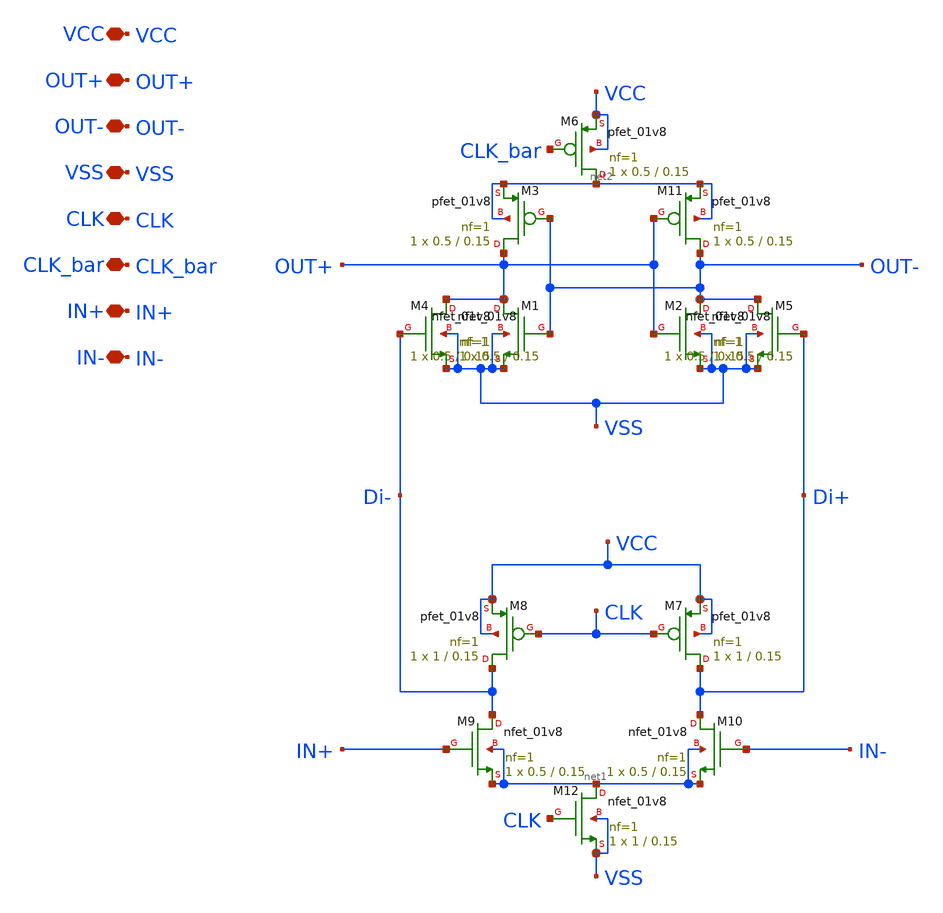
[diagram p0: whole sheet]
** sch_path: voltage_comp/double_tail_comp.sch
**.subckt double_tail_comp OUT- VSS VCC OUT+ IN+ IN- CLK CLK_bar
*.iopin OUT-
*.iopin VSS
*.iopin VCC
*.iopin OUT+
*.iopin IN+
*.iopin IN-
*.iopin CLK
*.iopin CLK_bar
XM2 OUT- OUT+ VSS VSS sky130_fd_pr__nfet_01v8 L=0.15 W=0.5 nf=1 ad='int((1 + 1)/2) * 0.5 / 1 * 0.29'
+ as='int((1 + 2)/2) * 0.5 / 1 * 0.29' pd='2*int((1 + 1)/2) * (0.5 / 1 + 0.29)' ps='2*int((1 + 2)/2) * (0.5 / 1 + 0.29)'
+ nrd='0.29 / 0.5 ' nrs='0.29 / 0.5 ' sa=0 sb=0 sd=0 mult=1 m=1
XM11 OUT- OUT+ net2 net2 sky130_fd_pr__pfet_01v8 L=0.15 W=0.5 nf=1 ad='int((nf+1)/2) * W/nf * 0.29' as='int((nf+2)/2) * W/nf * 0.29'
+ pd='2*int((nf+1)/2) * (W/nf + 0.29)' ps='2*int((nf+2)/2) * (W/nf + 0.29)' nrd='0.29 / W' nrs='0.29 / W'
+ sa=0 sb=0 sd=0 mult=1 m=1
XM1 OUT+ OUT- VSS VSS sky130_fd_pr__nfet_01v8 L=0.15 W=0.5 nf=1 ad='int((1 + 1)/2) * 0.5 / 1 * 0.29'
+ as='int((1 + 2)/2) * 0.5 / 1 * 0.29' pd='2*int((1 + 1)/2) * (0.5 / 1 + 0.29)' ps='2*int((1 + 2)/2) * (0.5 / 1 + 0.29)'
+ nrd='0.29 / 0.5 ' nrs='0.29 / 0.5 ' sa=0 sb=0 sd=0 mult=1 m=1
XM3 OUT+ OUT- net2 net2 sky130_fd_pr__pfet_01v8 L=0.15 W=0.5 nf=1 ad='int((nf+1)/2) * W/nf * 0.29' as='int((nf+2)/2) * W/nf * 0.29'
+ pd='2*int((nf+1)/2) * (W/nf + 0.29)' ps='2*int((nf+2)/2) * (W/nf + 0.29)' nrd='0.29 / W' nrs='0.29 / W'
+ sa=0 sb=0 sd=0 mult=1 m=1
XM4 OUT+ Di- VSS VSS sky130_fd_pr__nfet_01v8 L=0.15 W=0.5 nf=1 ad='int((1 + 1)/2) * 0.5 / 1 * 0.29' as='int((1 + 2)/2) * 0.5 / 1 * 0.29'
+ pd='2*int((1 + 1)/2) * (0.5 / 1 + 0.29)' ps='2*int((1 + 2)/2) * (0.5 / 1 + 0.29)' nrd='0.29 / 0.5 ' nrs='0.29 / 0.5 '
+ sa=0 sb=0 sd=0 mult=1 m=1
XM5 OUT- Di+ VSS VSS sky130_fd_pr__nfet_01v8 L=0.15 W=0.5 nf=1 ad='int((1 + 1)/2) * 0.5 / 1 * 0.29' as='int((1 + 2)/2) * 0.5 / 1 * 0.29'
+ pd='2*int((1 + 1)/2) * (0.5 / 1 + 0.29)' ps='2*int((1 + 2)/2) * (0.5 / 1 + 0.29)' nrd='0.29 / 0.5 ' nrs='0.29 / 0.5 '
+ sa=0 sb=0 sd=0 mult=1 m=1
XM6 net2 CLK_bar VCC VCC sky130_fd_pr__pfet_01v8 L=0.15 W=0.5 nf=1 ad='int((nf+1)/2) * W/nf * 0.29' as='int((nf+2)/2) * W/nf * 0.29'
+ pd='2*int((nf+1)/2) * (W/nf + 0.29)' ps='2*int((nf+2)/2) * (W/nf + 0.29)' nrd='0.29 / W' nrs='0.29 / W'
+ sa=0 sb=0 sd=0 mult=1 m=1
XM8 Di- CLK VCC VCC sky130_fd_pr__pfet_01v8 L=0.15 W=1 nf=1 ad='int((nf+1)/2) * W/nf * 0.29' as='int((nf+2)/2) * W/nf * 0.29'
+ pd='2*int((nf+1)/2) * (W/nf + 0.29)' ps='2*int((nf+2)/2) * (W/nf + 0.29)' nrd='0.29 / W' nrs='0.29 / W'
+ sa=0 sb=0 sd=0 mult=1 m=1
XM9 Di- IN+ net1 net1 sky130_fd_pr__nfet_01v8 L=0.15 W=0.5 nf=1 ad='int((1 + 1)/2) * 0.5 / 1 * 0.29'
+ as='int((1 + 2)/2) * 0.5 / 1 * 0.29' pd='2*int((1 + 1)/2) * (0.5 / 1 + 0.29)' ps='2*int((1 + 2)/2) * (0.5 / 1 + 0.29)'
+ nrd='0.29 / 0.5 ' nrs='0.29 / 0.5 ' sa=0 sb=0 sd=0 mult=1 m=1
XM7 Di+ CLK VCC VCC sky130_fd_pr__pfet_01v8 L=0.15 W=1 nf=1 ad='int((nf+1)/2) * W/nf * 0.29' as='int((nf+2)/2) * W/nf * 0.29'
+ pd='2*int((nf+1)/2) * (W/nf + 0.29)' ps='2*int((nf+2)/2) * (W/nf + 0.29)' nrd='0.29 / W' nrs='0.29 / W'
+ sa=0 sb=0 sd=0 mult=1 m=1
XM10 Di+ IN- net1 net1 sky130_fd_pr__nfet_01v8 L=0.15 W=0.5 nf=1 ad='int((1 + 1)/2) * 0.5 / 1 * 0.29'
+ as='int((1 + 2)/2) * 0.5 / 1 * 0.29' pd='2*int((1 + 1)/2) * (0.5 / 1 + 0.29)' ps='2*int((1 + 2)/2) * (0.5 / 1 + 0.29)'
+ nrd='0.29 / 0.5 ' nrs='0.29 / 0.5 ' sa=0 sb=0 sd=0 mult=1 m=1
XM12 net1 CLK VSS VSS sky130_fd_pr__nfet_01v8 L=0.15 W=1 nf=1 ad='int((1 + 1)/2) * 1 / 1 * 0.29' as='int((1 + 2)/2) * 1 / 1 * 0.29'
+ pd='2*int((1 + 1)/2) * (1 / 1 + 0.29)' ps='2*int((1 + 2)/2) * (1 / 1 + 0.29)' nrd='0.29 / 1 ' nrs='0.29 / 1 '
+ sa=0 sb=0 sd=0 mult=1 m=1
**.ends
.end
